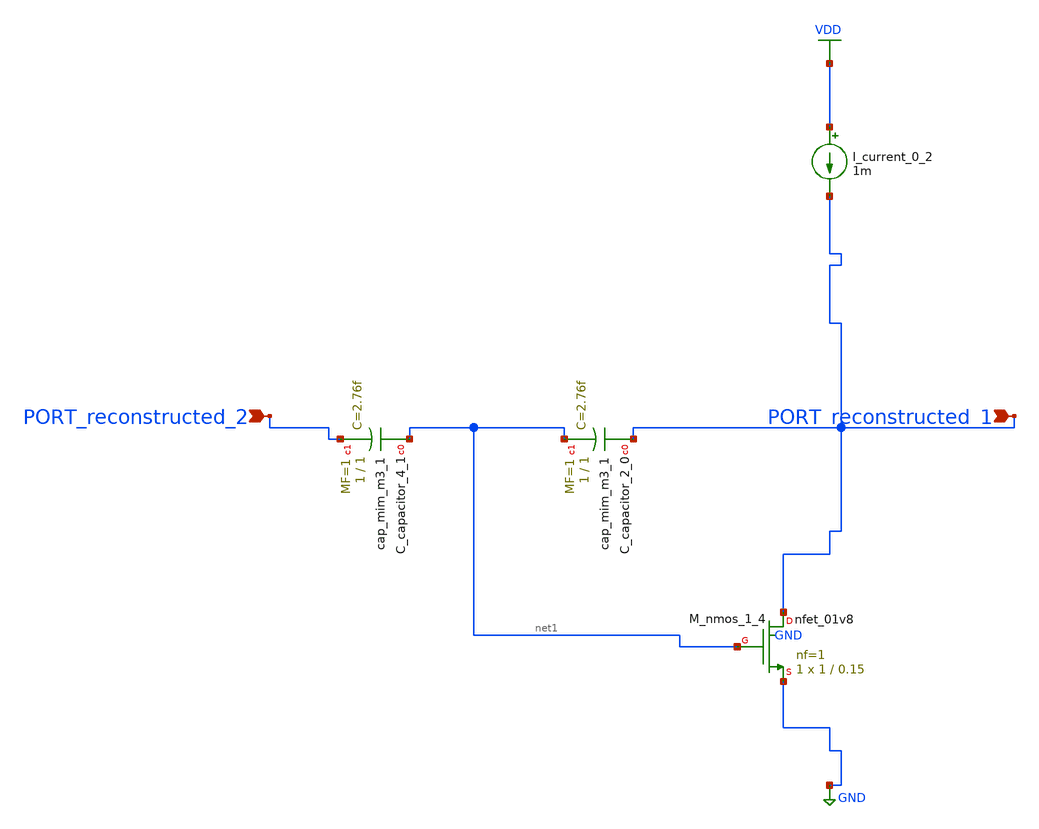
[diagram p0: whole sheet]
** sch_path: schematics/AMSNet/612.sch
**.subckt 612 PORT_reconstructed_1 PORT_reconstructed_2
*.ipin PORT_reconstructed_1
*.ipin PORT_reconstructed_2
XC_capacitor_2_0 PORT_reconstructed_1 net1 sky130_fd_pr__cap_mim_m3_1 W=1 L=1 MF=1 m=1
XC_capacitor_4_1 net1 PORT_reconstructed_2 sky130_fd_pr__cap_mim_m3_1 W=1 L=1 MF=1 m=1
I_current_0_2 VDD PORT_reconstructed_1 1m
XM_nmos_1_4 PORT_reconstructed_1 net1 GND GND sky130_fd_pr__nfet_01v8 L=0.15 W=1 nf=1 ad='int((1 + 1)/2) * 1 / 1 * 0.29'
+ as='int((1 + 2)/2) * 1 / 1 * 0.29' pd='2*int((1 + 1)/2) * (1 / 1 + 0.29)' ps='2*int((1 + 2)/2) * (1 / 1 + 0.29)'
+ nrd='0.29 / 1 ' nrs='0.29 / 1 ' sa=0 sb=0 sd=0 mult=1 m=1
**.ends
.GLOBAL GND
.GLOBAL VDD
.end
